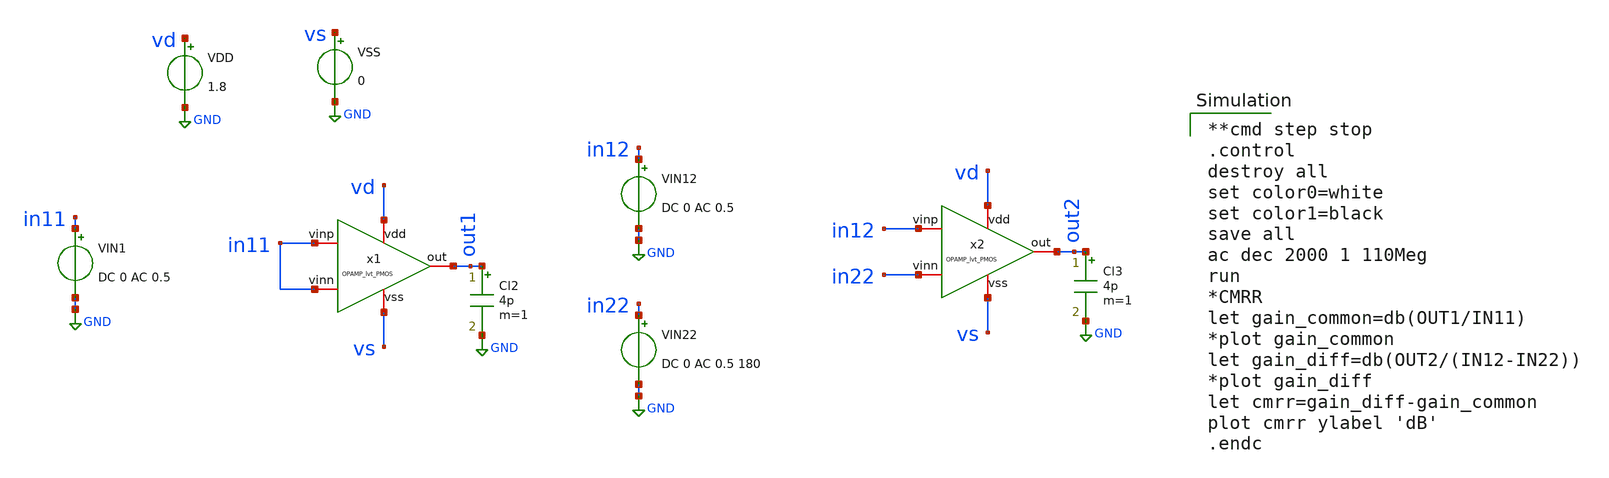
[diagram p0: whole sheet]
** sch_path: ANOTHER_SOLUTIONS_CONSIDERED/ANOTHER_BIAS_FOR_TEMPERATURE_SENSOR/OPAMP/XSCHEM/OPAMP_tb-CMRR.sch
**.subckt OPAMP_tb-CMRR
VDD vd GND 1.8
VSS vs GND 0
VIN12 in12 GND DC 0 AC 0.5
VIN22 in22 GND DC 0 AC 0.5 180
VIN1 in11 GND DC 0 AC 0.5
Cl2 out1 GND 4p m=1
Cl3 out2 GND 4p m=1
x1 vd in11 in11 out1 vs OPAMP_lvt_PMOS
x2 vd in22 in12 out2 vs OPAMP_lvt_PMOS
**** begin user architecture code

**cmd step stop
.control
destroy all
set color0=white
set color1=black
save all
ac dec 2000 1 110Meg
run
*CMRR
let gain_common=db(OUT1/IN11)
*plot gain_common
let gain_diff=db(OUT2/(IN12-IN22))
*plot gain_diff
let cmrr=gain_diff-gain_common
plot cmrr ylabel 'dB'
.endc

 .lib $::SKYWATER_MODELS/sky130.lib.spice tt
.include $::SKYWATER_STDCELLS/sky130_fd_sc_hd.spice

**** end user architecture code
**.ends

* expanding   symbol:  Documentos/TESIS DE GRADO/WORK_IN_PROGRESS/My_xschem/OPAMP_lvt_PMOS.sym # of
*+ pins=5
** sym_path: ANOTHER_SOLUTIONS_CONSIDERED/ANOTHER_BIAS_FOR_TEMPERATURE_SENSOR/OPAMP/XSCHEM/OPAMP_lvt_PMOS.sym
** sch_path: ANOTHER_SOLUTIONS_CONSIDERED/ANOTHER_BIAS_FOR_TEMPERATURE_SENSOR/OPAMP/XSCHEM/OPAMP_lvt_PMOS.sch
.subckt OPAMP_lvt_PMOS vdd vinn vinp out vss
*.iopin vdd
*.iopin vss
*.iopin out
*.iopin vinp
*.iopin vinn
XC1 net3 out sky130_fd_pr__cap_mim_m3_1 W=5 L=5 MF=1 m=1
XM1 net1 net4 vdd vdd sky130_fd_pr__pfet_01v8_lvt L=2 W=5 nf=1 ad='int((nf+1)/2) * W/nf * 0.29' as='int((nf+2)/2) * W/nf * 0.29'
+ pd='2*int((nf+1)/2) * (W/nf + 0.29)' ps='2*int((nf+2)/2) * (W/nf + 0.29)' nrd='0.29 / W' nrs='0.29 / W'
+ sa=0 sb=0 sd=0 mult=2 m=2
XM2 net2 vinn net1 vdd sky130_fd_pr__pfet_01v8_lvt L=2 W=5 nf=1 ad='int((nf+1)/2) * W/nf * 0.29' as='int((nf+2)/2) * W/nf * 0.29'
+ pd='2*int((nf+1)/2) * (W/nf + 0.29)' ps='2*int((nf+2)/2) * (W/nf + 0.29)' nrd='0.29 / W' nrs='0.29 / W'
+ sa=0 sb=0 sd=0 mult=4 m=4
XM3 net3 vinp net1 vdd sky130_fd_pr__pfet_01v8_lvt L=2 W=5 nf=1 ad='int((nf+1)/2) * W/nf * 0.29' as='int((nf+2)/2) * W/nf * 0.29'
+ pd='2*int((nf+1)/2) * (W/nf + 0.29)' ps='2*int((nf+2)/2) * (W/nf + 0.29)' nrd='0.29 / W' nrs='0.29 / W'
+ sa=0 sb=0 sd=0 mult=4 m=4
XM4 net2 net2 vss vss sky130_fd_pr__nfet_01v8_lvt L=2 W=2 nf=1 ad='int((nf+1)/2) * W/nf * 0.29' as='int((nf+2)/2) * W/nf * 0.29'
+ pd='2*int((nf+1)/2) * (W/nf + 0.29)' ps='2*int((nf+2)/2) * (W/nf + 0.29)' nrd='0.29 / W' nrs='0.29 / W'
+ sa=0 sb=0 sd=0 mult=2 m=2
XM5 net3 net2 vss vss sky130_fd_pr__nfet_01v8_lvt L=2 W=2 nf=1 ad='int((nf+1)/2) * W/nf * 0.29' as='int((nf+2)/2) * W/nf * 0.29'
+ pd='2*int((nf+1)/2) * (W/nf + 0.29)' ps='2*int((nf+2)/2) * (W/nf + 0.29)' nrd='0.29 / W' nrs='0.29 / W'
+ sa=0 sb=0 sd=0 mult=2 m=2
XM6 out net4 vdd vdd sky130_fd_pr__pfet_01v8_lvt L=2 W=10 nf=2 ad='int((nf+1)/2) * W/nf * 0.29' as='int((nf+2)/2) * W/nf * 0.29'
+ pd='2*int((nf+1)/2) * (W/nf + 0.29)' ps='2*int((nf+2)/2) * (W/nf + 0.29)' nrd='0.29 / W' nrs='0.29 / W'
+ sa=0 sb=0 sd=0 mult=1 m=1
XM7 out net3 vss vss sky130_fd_pr__nfet_01v8_lvt L=2 W=2 nf=1 ad='int((nf+1)/2) * W/nf * 0.29' as='int((nf+2)/2) * W/nf * 0.29'
+ pd='2*int((nf+1)/2) * (W/nf + 0.29)' ps='2*int((nf+2)/2) * (W/nf + 0.29)' nrd='0.29 / W' nrs='0.29 / W'
+ sa=0 sb=0 sd=0 mult=3 m=3
XM8 net4 net4 vdd vdd sky130_fd_pr__pfet_01v8_lvt L=2 W=5 nf=1 ad='int((nf+1)/2) * W/nf * 0.29' as='int((nf+2)/2) * W/nf * 0.29'
+ pd='2*int((nf+1)/2) * (W/nf + 0.29)' ps='2*int((nf+2)/2) * (W/nf + 0.29)' nrd='0.29 / W' nrs='0.29 / W'
+ sa=0 sb=0 sd=0 mult=2 m=2
XM9 net4 net4 vss vss sky130_fd_pr__nfet_01v8_lvt L=2 W=2 nf=1 ad='int((nf+1)/2) * W/nf * 0.29' as='int((nf+2)/2) * W/nf * 0.29'
+ pd='2*int((nf+1)/2) * (W/nf + 0.29)' ps='2*int((nf+2)/2) * (W/nf + 0.29)' nrd='0.29 / W' nrs='0.29 / W'
+ sa=0 sb=0 sd=0 mult=2 m=2
.ends

.GLOBAL GND
.end
